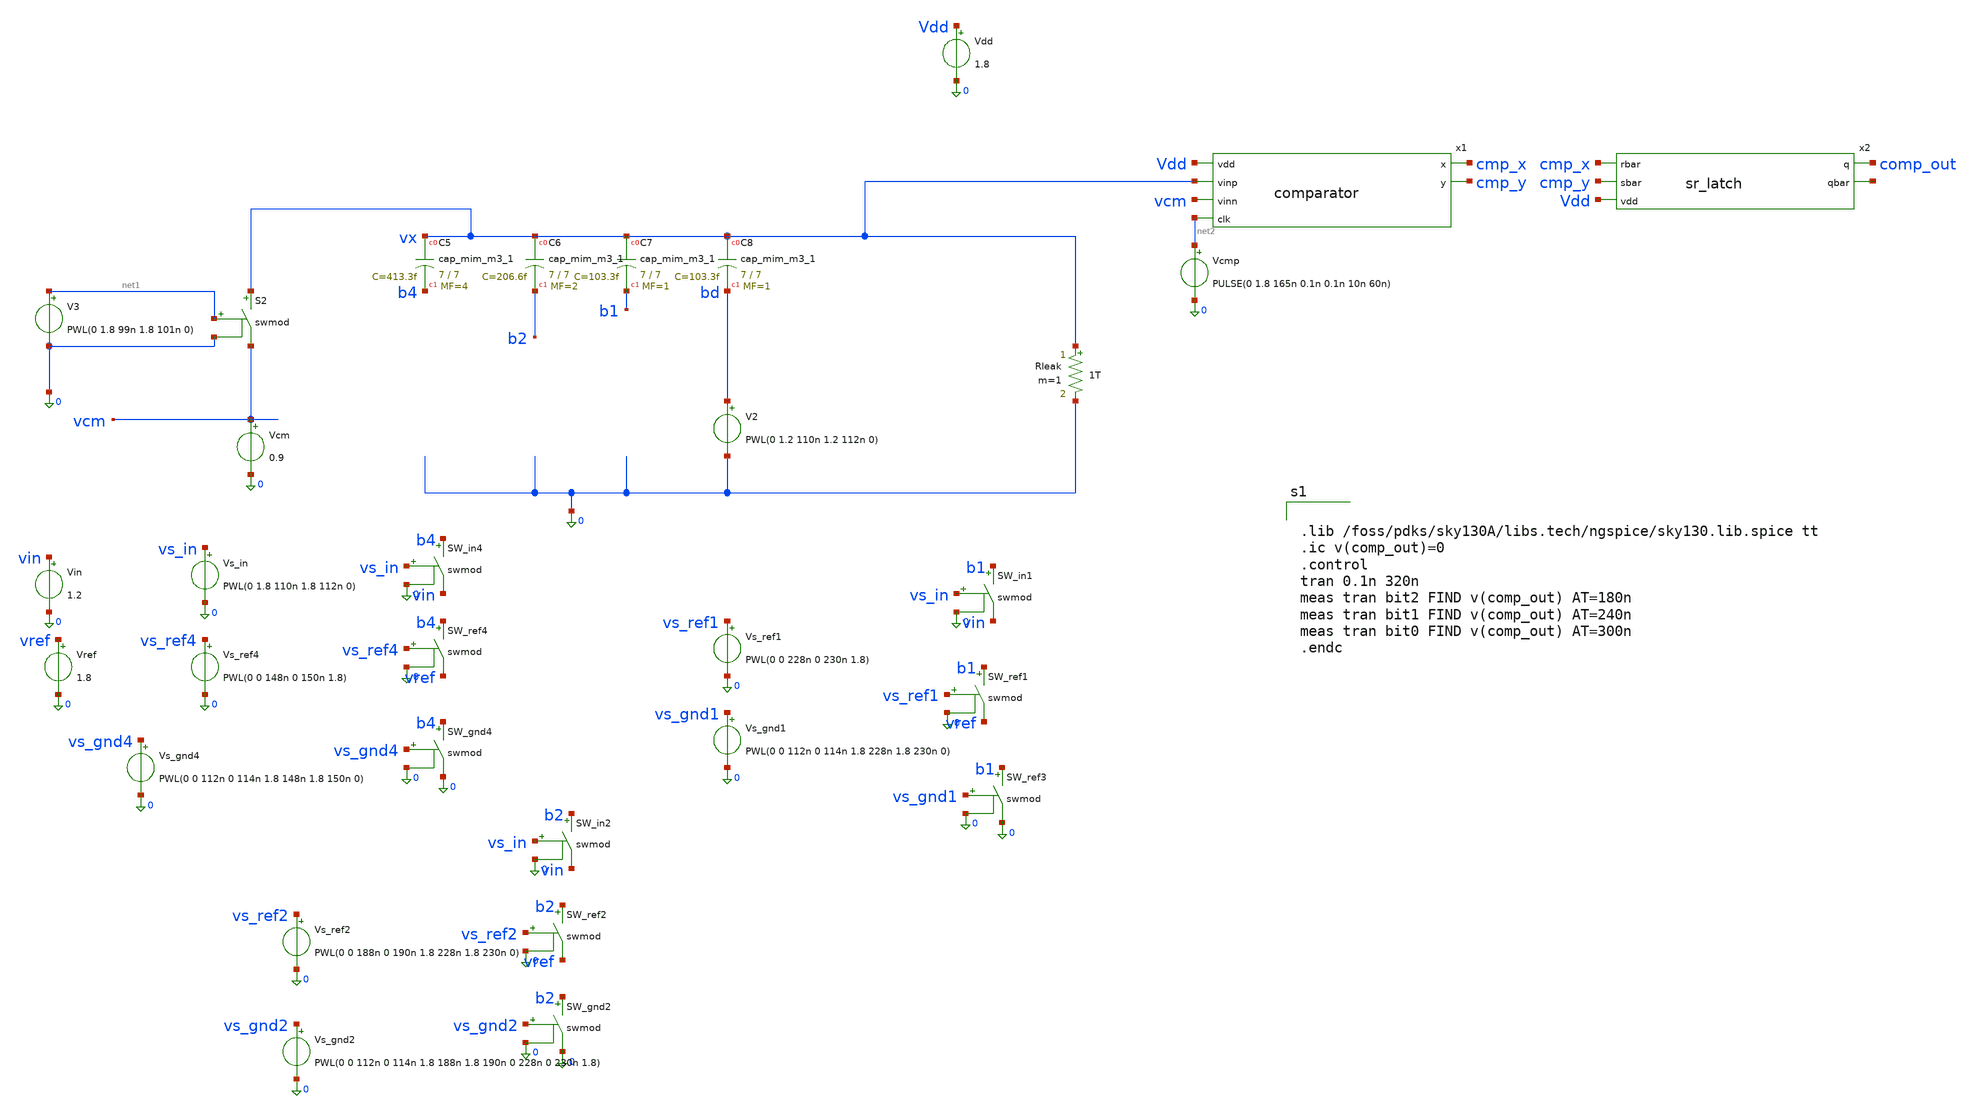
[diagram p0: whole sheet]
** sch_path: sch/cap_array.sch
**.subckt cap_array
V2 bd 0 PWL(0 1.2 110n 1.2 112n 0)
V3 net1 0 PWL(0 1.8 99n 1.8 101n 0)
S2 vx vcm net1 0 swmod
Rleak vx 0 1T m=1
x1 Vdd cmp_x cmp_y vx vcm net2 comparator
Vcmp net2 0 PULSE(0 1.8 165n 0.1n 0.1n 10n 60n)
Vdd Vdd 0 1.8
Vcm vcm 0 0.9
Vin vin 0 1.2
Vref vref 0 1.8
SW_in4 b4 vin vs_in 0 swmod
SW_gnd4 b4 0 vs_gnd4 0 swmod
SW_ref4 b4 vref vs_ref4 0 swmod
Vs_in vs_in 0 PWL(0 1.8 110n 1.8 112n 0)
Vs_ref4 vs_ref4 0 PWL(0 0 148n 0 150n 1.8)
Vs_gnd4 vs_gnd4 0 PWL(0 0 112n 0 114n 1.8 148n 1.8 150n 0)
SW_ref2 b2 vref vs_ref2 0 swmod
SW_in2 b2 vin vs_in 0 swmod
SW_gnd2 b2 0 vs_gnd2 0 swmod
Vs_ref2 vs_ref2 0 PWL(0 0 188n 0 190n 1.8 228n 1.8 230n 0)
Vs_gnd2 vs_gnd2 0 PWL(0 0 112n 0 114n 1.8 188n 1.8 190n 0 228n 0 230n 1.8)
SW_in1 b1 vin vs_in 0 swmod
SW_ref1 b1 vref vs_ref1 0 swmod
SW_ref3 b1 0 vs_gnd1 0 swmod
Vs_ref1 vs_ref1 0 PWL(0 0 228n 0 230n 1.8)
Vs_gnd1 vs_gnd1 0 PWL(0 0 112n 0 114n 1.8 228n 1.8 230n 0)
x2 cmp_x cmp_y Vdd comp_out net3 sr_latch
XC5 vx b4 sky130_fd_pr__cap_mim_m3_1 W=7 L=7 MF=4 m=4
XC6 vx b2 sky130_fd_pr__cap_mim_m3_1 W=7 L=7 MF=2 m=2
XC7 vx b1 sky130_fd_pr__cap_mim_m3_1 W=7 L=7 MF=1 m=1
XC8 vx bd sky130_fd_pr__cap_mim_m3_1 W=7 L=7 MF=1 m=1
**** begin user architecture code


.lib /foss/pdks/sky130A/libs.tech/ngspice/sky130.lib.spice tt
.ic v(comp_out)=0
.control
tran 0.1n 320n
meas tran bit2 FIND v(comp_out) AT=180n
meas tran bit1 FIND v(comp_out) AT=240n
meas tran bit0 FIND v(comp_out) AT=300n
.endc


**** end user architecture code
**.ends

* expanding   symbol:  comparator.sym # of pins=6
** sym_path: sch/comparator.sym
** sch_path: sch/comparator.sch
.subckt comparator vdd x y vinp vinn clk
*.ipin vinp
*.ipin vinn
*.opin y
*.opin x
*.ipin vdd
*.ipin clk
XM1 p vinp net1 0 sky130_fd_pr__nfet_01v8 L=0.5 W=4 nf=1 ad='int((1 + 1)/2) * 4 / 1 * 0.29' as='int((1 + 2)/2) * 4 / 1 * 0.29'
+ pd='2*int((1 + 1)/2) * (4 / 1 + 0.29)' ps='2*int((1 + 2)/2) * (4 / 1 + 0.29)' nrd='0.29 / 4 ' nrs='0.29 / 4 '
+ sa=0 sb=0 sd=0 mult=1 m=1
XM2 q vinn net1 0 sky130_fd_pr__nfet_01v8 L=0.5 W=4 nf=1 ad='int((1 + 1)/2) * 4 / 1 * 0.29' as='int((1 + 2)/2) * 4 / 1 * 0.29'
+ pd='2*int((1 + 1)/2) * (4 / 1 + 0.29)' ps='2*int((1 + 2)/2) * (4 / 1 + 0.29)' nrd='0.29 / 4 ' nrs='0.29 / 4 '
+ sa=0 sb=0 sd=0 mult=1 m=1
XMtail net1 clk 0 0 sky130_fd_pr__nfet_01v8 L=0.5 W=8 nf=1 ad='int((1 + 1)/2) * 8 / 1 * 0.29' as='int((1 + 2)/2) * 8 / 1 * 0.29'
+ pd='2*int((1 + 1)/2) * (8 / 1 + 0.29)' ps='2*int((1 + 2)/2) * (8 / 1 + 0.29)' nrd='0.29 / 8 ' nrs='0.29 / 8 '
+ sa=0 sb=0 sd=0 mult=1 m=1
XM4 y x q 0 sky130_fd_pr__nfet_01v8 L=0.15 W=1 nf=1 ad='int((1 + 1)/2) * 1 / 1 * 0.29' as='int((1 + 2)/2) * 1 / 1 * 0.29'
+ pd='2*int((1 + 1)/2) * (1 / 1 + 0.29)' ps='2*int((1 + 2)/2) * (1 / 1 + 0.29)' nrd='0.29 / 1 ' nrs='0.29 / 1 '
+ sa=0 sb=0 sd=0 mult=1 m=1
XM3 x y p 0 sky130_fd_pr__nfet_01v8 L=0.15 W=1 nf=1 ad='int((1 + 1)/2) * 1 / 1 * 0.29' as='int((1 + 2)/2) * 1 / 1 * 0.29'
+ pd='2*int((1 + 1)/2) * (1 / 1 + 0.29)' ps='2*int((1 + 2)/2) * (1 / 1 + 0.29)' nrd='0.29 / 1 ' nrs='0.29 / 1 '
+ sa=0 sb=0 sd=0 mult=1 m=1
XM5 x y vdd vdd sky130_fd_pr__pfet_01v8 L=0.15 W=2 nf=1 ad='int((1 + 1)/2) * 2 / 1 * 0.29' as='int((1 + 2)/2) * 2 / 1 * 0.29'
+ pd='2*int((1 + 1)/2) * (2 / 1 + 0.29)' ps='2*int((1 + 2)/2) * (2 / 1 + 0.29)' nrd='0.29 / 2 ' nrs='0.29 / 2 '
+ sa=0 sb=0 sd=0 mult=1 m=1
XM6 y x vdd vdd sky130_fd_pr__pfet_01v8 L=0.15 W=2 nf=1 ad='int((1 + 1)/2) * 2 / 1 * 0.29' as='int((1 + 2)/2) * 2 / 1 * 0.29'
+ pd='2*int((1 + 1)/2) * (2 / 1 + 0.29)' ps='2*int((1 + 2)/2) * (2 / 1 + 0.29)' nrd='0.29 / 2 ' nrs='0.29 / 2 '
+ sa=0 sb=0 sd=0 mult=1 m=1
XSw1 p clk vdd vdd sky130_fd_pr__pfet_01v8 L=0.15 W=2 nf=1 ad='int((1 + 1)/2) * 2 / 1 * 0.29' as='int((1 + 2)/2) * 2 / 1 * 0.29'
+ pd='2*int((1 + 1)/2) * (2 / 1 + 0.29)' ps='2*int((1 + 2)/2) * (2 / 1 + 0.29)' nrd='0.29 / 2 ' nrs='0.29 / 2 '
+ sa=0 sb=0 sd=0 mult=1 m=1
XSw3 x clk vdd vdd sky130_fd_pr__pfet_01v8 L=0.15 W=2 nf=1 ad='int((1 + 1)/2) * 2 / 1 * 0.29' as='int((1 + 2)/2) * 2 / 1 * 0.29'
+ pd='2*int((1 + 1)/2) * (2 / 1 + 0.29)' ps='2*int((1 + 2)/2) * (2 / 1 + 0.29)' nrd='0.29 / 2 ' nrs='0.29 / 2 '
+ sa=0 sb=0 sd=0 mult=1 m=1
XSw2 y clk vdd vdd sky130_fd_pr__pfet_01v8 L=0.15 W=2 nf=1 ad='int((1 + 1)/2) * 2 / 1 * 0.29' as='int((1 + 2)/2) * 2 / 1 * 0.29'
+ pd='2*int((1 + 1)/2) * (2 / 1 + 0.29)' ps='2*int((1 + 2)/2) * (2 / 1 + 0.29)' nrd='0.29 / 2 ' nrs='0.29 / 2 '
+ sa=0 sb=0 sd=0 mult=1 m=1
XSw4 q clk vdd vdd sky130_fd_pr__pfet_01v8 L=0.15 W=2 nf=1 ad='int((1 + 1)/2) * 2 / 1 * 0.29' as='int((1 + 2)/2) * 2 / 1 * 0.29'
+ pd='2*int((1 + 1)/2) * (2 / 1 + 0.29)' ps='2*int((1 + 2)/2) * (2 / 1 + 0.29)' nrd='0.29 / 2 ' nrs='0.29 / 2 '
+ sa=0 sb=0 sd=0 mult=1 m=1
.ends


* expanding   symbol:  sr_latch.sym # of pins=5
** sym_path: sch/sr_latch.sym
** sch_path: sch/sr_latch.sch
.subckt sr_latch rbar sbar vdd q qbar
*.ipin rbar
*.ipin sbar
*.ipin vdd
*.opin q
*.opin qbar
x1 vdd q sbar qbar nand2
x2 vdd qbar rbar q nand2
.ends


* expanding   symbol:  nand2.sym # of pins=4
** sym_path: sch/nand2.sym
** sch_path: sch/nand2.sch
.subckt nand2 vdd y a b
*.ipin a
*.ipin vdd
*.opin y
*.ipin b
XP1 y a vdd vdd sky130_fd_pr__pfet_01v8 L=0.15 W=2 nf=1 ad='int((1 + 1)/2) * 2 / 1 * 0.29' as='int((1 + 2)/2) * 2 / 1 * 0.29'
+ pd='2*int((1 + 1)/2) * (2 / 1 + 0.29)' ps='2*int((1 + 2)/2) * (2 / 1 + 0.29)' nrd='0.29 / 2 ' nrs='0.29 / 2 '
+ sa=0 sb=0 sd=0 mult=1 m=1
XP2 y b vdd vdd sky130_fd_pr__pfet_01v8 L=0.15 W=2 nf=1 ad='int((1 + 1)/2) * 2 / 1 * 0.29' as='int((1 + 2)/2) * 2 / 1 * 0.29'
+ pd='2*int((1 + 1)/2) * (2 / 1 + 0.29)' ps='2*int((1 + 2)/2) * (2 / 1 + 0.29)' nrd='0.29 / 2 ' nrs='0.29 / 2 '
+ sa=0 sb=0 sd=0 mult=1 m=1
XN1 y a net1 0 sky130_fd_pr__nfet_01v8 L=0.15 W=2 nf=1 ad='int((1 + 1)/2) * 2 / 1 * 0.29' as='int((1 + 2)/2) * 2 / 1 * 0.29'
+ pd='2*int((1 + 1)/2) * (2 / 1 + 0.29)' ps='2*int((1 + 2)/2) * (2 / 1 + 0.29)' nrd='0.29 / 2 ' nrs='0.29 / 2 '
+ sa=0 sb=0 sd=0 mult=1 m=1
XN2 net1 b 0 0 sky130_fd_pr__nfet_01v8 L=0.15 W=2 nf=1 ad='int((1 + 1)/2) * 2 / 1 * 0.29' as='int((1 + 2)/2) * 2 / 1 * 0.29'
+ pd='2*int((1 + 1)/2) * (2 / 1 + 0.29)' ps='2*int((1 + 2)/2) * (2 / 1 + 0.29)' nrd='0.29 / 2 ' nrs='0.29 / 2 '
+ sa=0 sb=0 sd=0 mult=1 m=1
.ends

**** begin user architecture code
.MODEL swmod SW   VT=0.9 VH=0.01  RON=0.01 ROFF=10G
**** end user architecture code
.end
